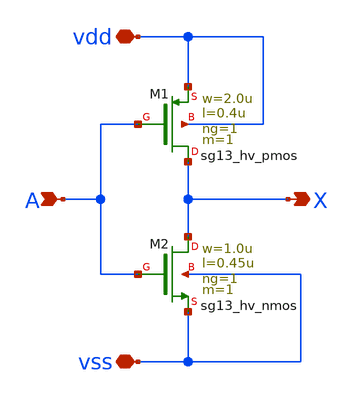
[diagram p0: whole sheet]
** sch_path: xschem/hv_inv_1.sch
**.subckt hv_inv_1 A vdd vss X
*.ipin A
*.iopin vdd
*.iopin vss
*.opin X
XM1 X A vdd vdd sg13_hv_pmos w=2.0u l=0.4u ng=1 m=1 mm_ok=1
XM2 X A vss vss sg13_hv_nmos w=1.0u l=0.45u ng=1 m=1 mm_ok=1
**.ends
.end
